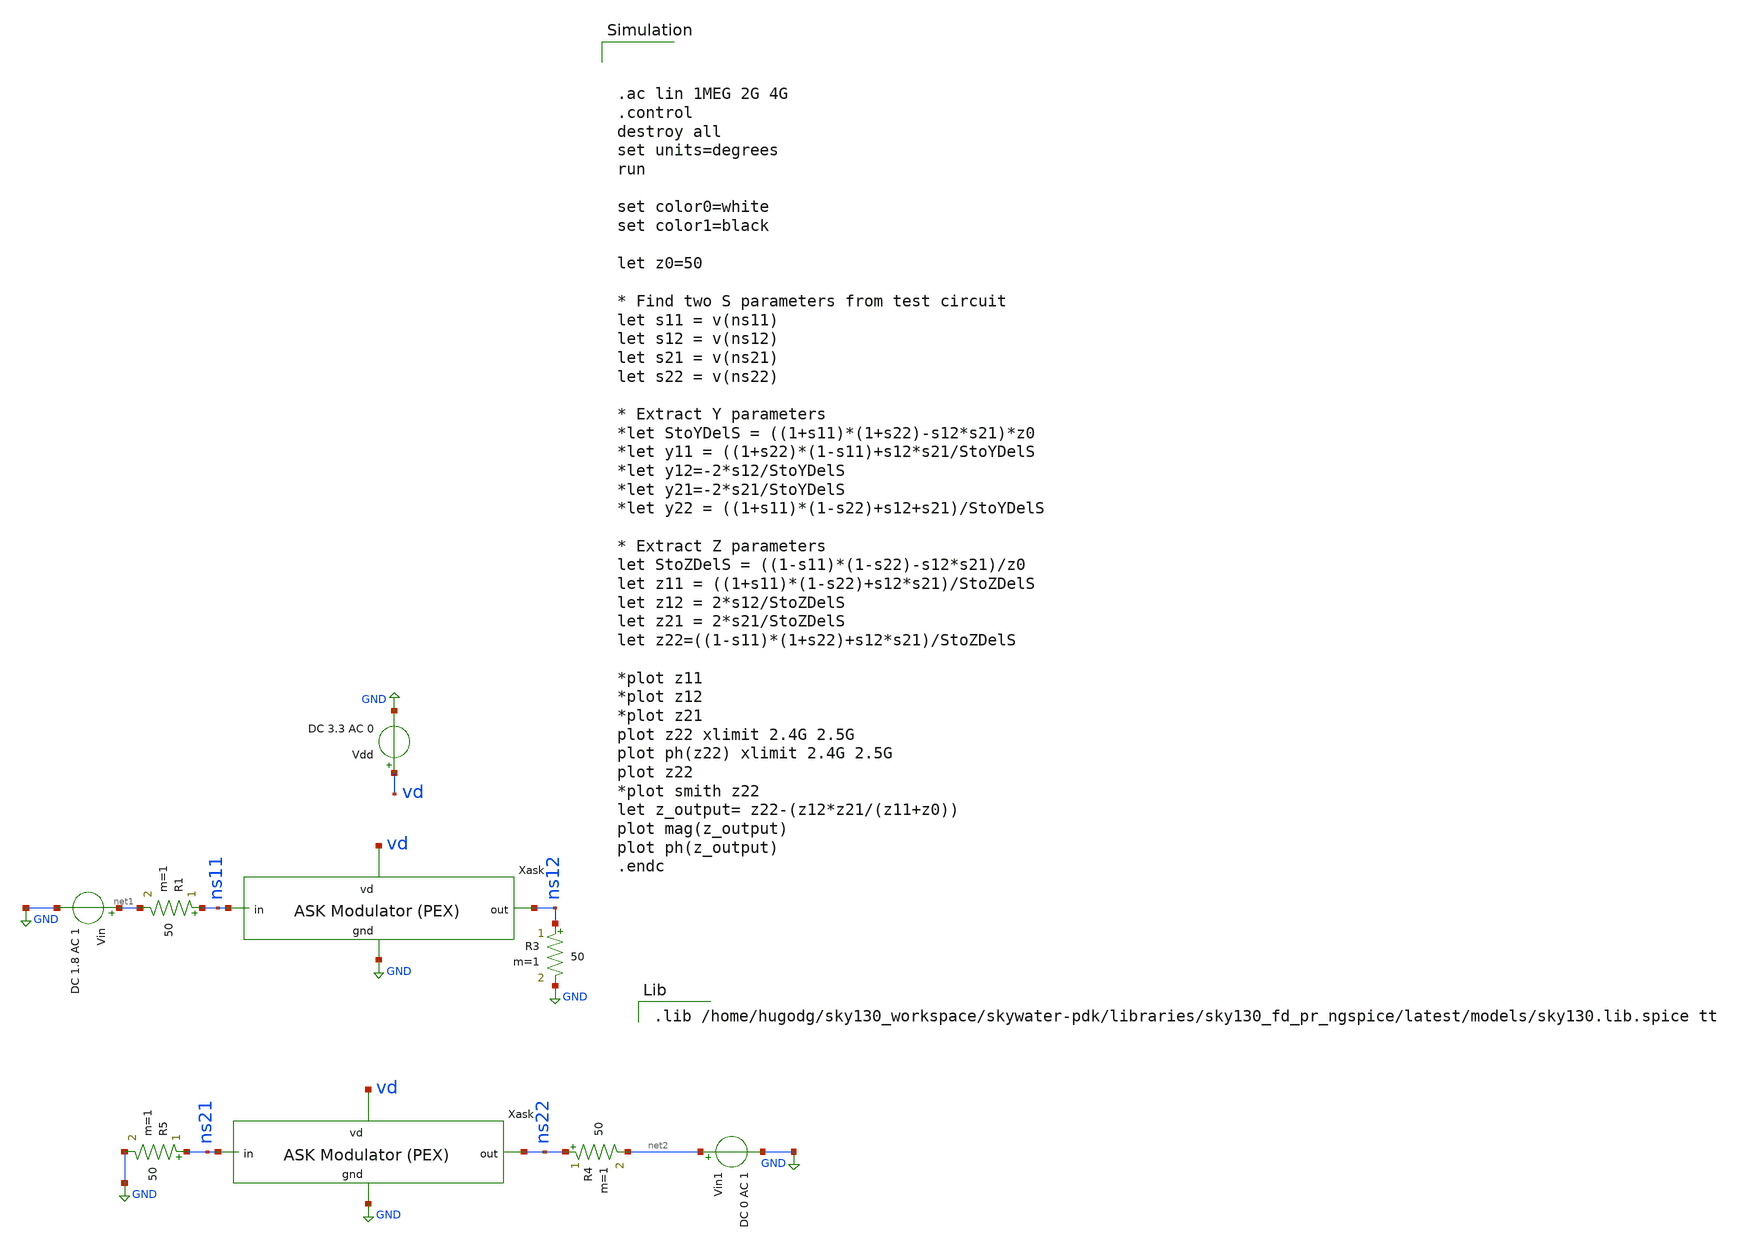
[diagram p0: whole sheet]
** sch_path: xschem/ask-modulator-pex_tb-ac.sch
**.subckt ask-modulator-pex_tb-ac
Vdd vd GND DC 3.3 AC 0
Vin net1 GND DC 1.8 AC 1
Vin1 net2 GND DC 0 AC 1
R1 ns11 net1 50 m=1
R3 ns12 GND 50 m=1
R4 ns22 net2 50 m=1
R5 ns21 GND 50 m=1
x1 vd ns12 ns11 GND ask-modulator-pex
x2 vd ns22 ns21 GND ask-modulator-pex
**** begin user architecture code



.ac lin 1MEG 2G 4G
.control
destroy all
set units=degrees
run

set color0=white
set color1=black

let z0=50

* Find two S parameters from test circuit
let s11 = v(ns11)
let s12 = v(ns12)
let s21 = v(ns21)
let s22 = v(ns22)

* Extract Y parameters
*let StoYDelS = ((1+s11)*(1+s22)-s12*s21)*z0
*let y11 = ((1+s22)*(1-s11)+s12*s21/StoYDelS
*let y12=-2*s12/StoYDelS
*let y21=-2*s21/StoYDelS
*let y22 = ((1+s11)*(1-s22)+s12+s21)/StoYDelS

* Extract Z parameters
let StoZDelS = ((1-s11)*(1-s22)-s12*s21)/z0
let z11 = ((1+s11)*(1-s22)+s12*s21)/StoZDelS
let z12 = 2*s12/StoZDelS
let z21 = 2*s21/StoZDelS
let z22=((1-s11)*(1+s22)+s12*s21)/StoZDelS

*plot z11
*plot z12
*plot z21
plot z22 xlimit 2.4G 2.5G
plot ph(z22) xlimit 2.4G 2.5G
plot z22
*plot smith z22
let z_output= z22-(z12*z21/(z11+z0))
plot mag(z_output)
plot ph(z_output)
.endc


.lib /home/hugodg/sky130_workspace/skywater-pdk/libraries/sky130_fd_pr_ngspice/latest/models/sky130.lib.spice tt

**** end user architecture code
**.ends
.GLOBAL GND
.end
